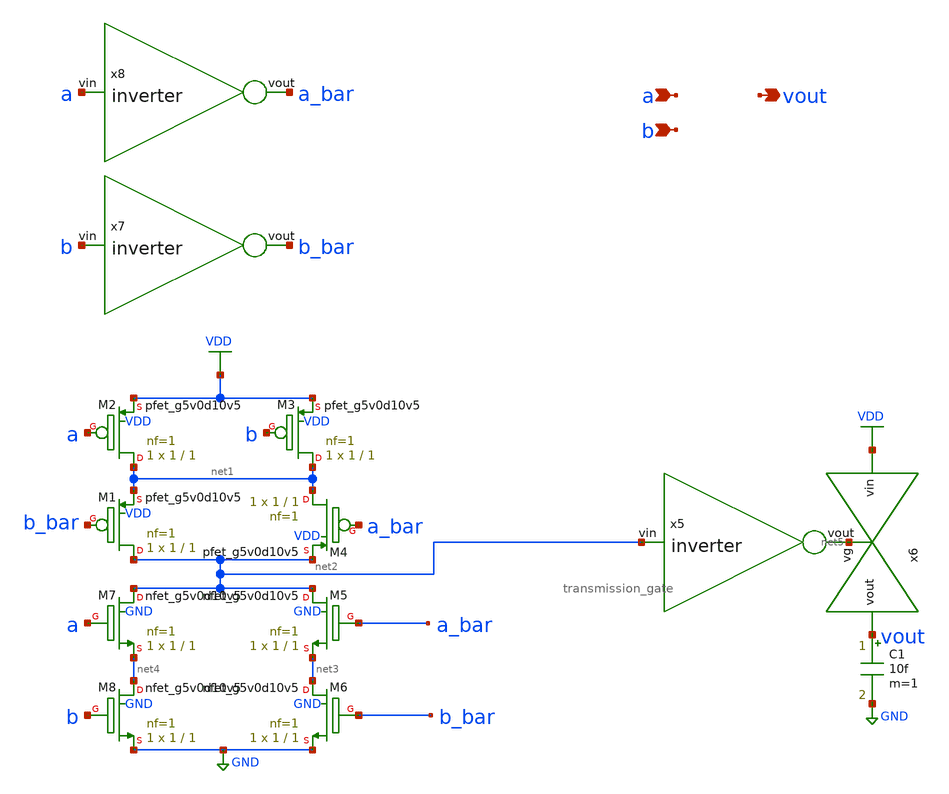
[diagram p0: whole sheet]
** sch_path: schematics/nxor.sch
**.subckt nxor a b vout
*.ipin a
*.ipin b
*.opin vout
XM2 net1 a VDD VDD sky130_fd_pr__pfet_g5v0d10v5 L=1 W=1 nf=1 ad='int((nf+1)/2) * W/nf * 0.29' as='int((nf+2)/2) * W/nf * 0.29'
+ pd='2*int((nf+1)/2) * (W/nf + 0.29)' ps='2*int((nf+2)/2) * (W/nf + 0.29)' nrd='0.29 / W' nrs='0.29 / W'
+ sa=0 sb=0 sd=0 mult=1 m=1
XM3 net1 b VDD VDD sky130_fd_pr__pfet_g5v0d10v5 L=1 W=1 nf=1 ad='int((nf+1)/2) * W/nf * 0.29' as='int((nf+2)/2) * W/nf * 0.29'
+ pd='2*int((nf+1)/2) * (W/nf + 0.29)' ps='2*int((nf+2)/2) * (W/nf + 0.29)' nrd='0.29 / W' nrs='0.29 / W'
+ sa=0 sb=0 sd=0 mult=1 m=1
XM8 net4 b GND GND sky130_fd_pr__nfet_g5v0d10v5 L=1 W=1 nf=1 ad='int((nf+1)/2) * W/nf * 0.29' as='int((nf+2)/2) * W/nf * 0.29'
+ pd='2*int((nf+1)/2) * (W/nf + 0.29)' ps='2*int((nf+2)/2) * (W/nf + 0.29)' nrd='0.29 / W' nrs='0.29 / W'
+ sa=0 sb=0 sd=0 mult=1 m=1
XM7 net2 a net4 GND sky130_fd_pr__nfet_g5v0d10v5 L=1 W=1 nf=1 ad='int((nf+1)/2) * W/nf * 0.29' as='int((nf+2)/2) * W/nf * 0.29'
+ pd='2*int((nf+1)/2) * (W/nf + 0.29)' ps='2*int((nf+2)/2) * (W/nf + 0.29)' nrd='0.29 / W' nrs='0.29 / W'
+ sa=0 sb=0 sd=0 mult=1 m=1
XM1 net2 b_bar net1 VDD sky130_fd_pr__pfet_g5v0d10v5 L=1 W=1 nf=1 ad='int((nf+1)/2) * W/nf * 0.29' as='int((nf+2)/2) * W/nf * 0.29'
+ pd='2*int((nf+1)/2) * (W/nf + 0.29)' ps='2*int((nf+2)/2) * (W/nf + 0.29)' nrd='0.29 / W' nrs='0.29 / W'
+ sa=0 sb=0 sd=0 mult=1 m=1
XM4 net1 a_bar net2 VDD sky130_fd_pr__pfet_g5v0d10v5 L=1 W=1 nf=1 ad='int((nf+1)/2) * W/nf * 0.29' as='int((nf+2)/2) * W/nf * 0.29'
+ pd='2*int((nf+1)/2) * (W/nf + 0.29)' ps='2*int((nf+2)/2) * (W/nf + 0.29)' nrd='0.29 / W' nrs='0.29 / W'
+ sa=0 sb=0 sd=0 mult=1 m=1
XM5 net2 a_bar net3 GND sky130_fd_pr__nfet_g5v0d10v5 L=1 W=1 nf=1 ad='int((nf+1)/2) * W/nf * 0.29' as='int((nf+2)/2) * W/nf * 0.29'
+ pd='2*int((nf+1)/2) * (W/nf + 0.29)' ps='2*int((nf+2)/2) * (W/nf + 0.29)' nrd='0.29 / W' nrs='0.29 / W'
+ sa=0 sb=0 sd=0 mult=1 m=1
XM6 net3 b_bar GND GND sky130_fd_pr__nfet_g5v0d10v5 L=1 W=1 nf=1 ad='int((nf+1)/2) * W/nf * 0.29' as='int((nf+2)/2) * W/nf * 0.29'
+ pd='2*int((nf+1)/2) * (W/nf + 0.29)' ps='2*int((nf+2)/2) * (W/nf + 0.29)' nrd='0.29 / W' nrs='0.29 / W'
+ sa=0 sb=0 sd=0 mult=1 m=1
x5 net5 net2 inverter
x6 VDD vout net5 transmission_gate
C1 vout GND 10f m=1
x7 b_bar b inverter
x8 a_bar a inverter
**.ends

* expanding   symbol:  /media/sf_share/final_project/inverter.sym # of pins=2
** sym_path: schematics/inverter.sym
** sch_path: schematics/inverter.sch
.subckt inverter vout vin
*.ipin vin
*.opin vout
XM3 vout vin VDD VDD sky130_fd_pr__pfet_g5v0d10v5 L=0.5 W=0.5 nf=1 ad='int((nf+1)/2) * W/nf * 0.29' as='int((nf+2)/2) * W/nf * 0.29'
+ pd='2*int((nf+1)/2) * (W/nf + 0.29)' ps='2*int((nf+2)/2) * (W/nf + 0.29)' nrd='0.29 / W' nrs='0.29 / W'
+ sa=0 sb=0 sd=0 mult=1 m=1
XM5 vout vin GND GND sky130_fd_pr__nfet_g5v0d10v5 L=0.5 W=0.5 nf=1 ad='int((nf+1)/2) * W/nf * 0.29' as='int((nf+2)/2) * W/nf * 0.29'
+ pd='2*int((nf+1)/2) * (W/nf + 0.29)' ps='2*int((nf+2)/2) * (W/nf + 0.29)' nrd='0.29 / W' nrs='0.29 / W'
+ sa=0 sb=0 sd=0 mult=1 m=1
.ends


* expanding   symbol:  /media/sf_share/final_project/transmission_gate.sym # of pins=3
** sym_path: schematics/transmission_gate.sym
** sch_path: schematics/transmission_gate.sch
.subckt transmission_gate vin vout vg
*.ipin vin
*.ipin vg
*.opin vout
x1 vg_bar vg inverter
XM5 vin vg vout GND sky130_fd_pr__nfet_g5v0d10v5 L=0.5 W=0.5 nf=1 ad='int((nf+1)/2) * W/nf * 0.29' as='int((nf+2)/2) * W/nf * 0.29'
+ pd='2*int((nf+1)/2) * (W/nf + 0.29)' ps='2*int((nf+2)/2) * (W/nf + 0.29)' nrd='0.29 / W' nrs='0.29 / W'
+ sa=0 sb=0 sd=0 mult=1 m=1
XM7 vout vg_bar vin VDD sky130_fd_pr__pfet_g5v0d10v5 L=0.5 W=0.5 nf=1 ad='int((nf+1)/2) * W/nf * 0.29'
+ as='int((nf+2)/2) * W/nf * 0.29' pd='2*int((nf+1)/2) * (W/nf + 0.29)' ps='2*int((nf+2)/2) * (W/nf + 0.29)'
+ nrd='0.29 / W' nrs='0.29 / W' sa=0 sb=0 sd=0 mult=1 m=1
XM6 vout vg_bar GND GND sky130_fd_pr__nfet_g5v0d10v5 L=0.5 W=0.5 nf=1 ad='int((nf+1)/2) * W/nf * 0.29'
+ as='int((nf+2)/2) * W/nf * 0.29' pd='2*int((nf+1)/2) * (W/nf + 0.29)' ps='2*int((nf+2)/2) * (W/nf + 0.29)'
+ nrd='0.29 / W' nrs='0.29 / W' sa=0 sb=0 sd=0 mult=1 m=1
.ends

.GLOBAL VDD
.GLOBAL GND
.end
